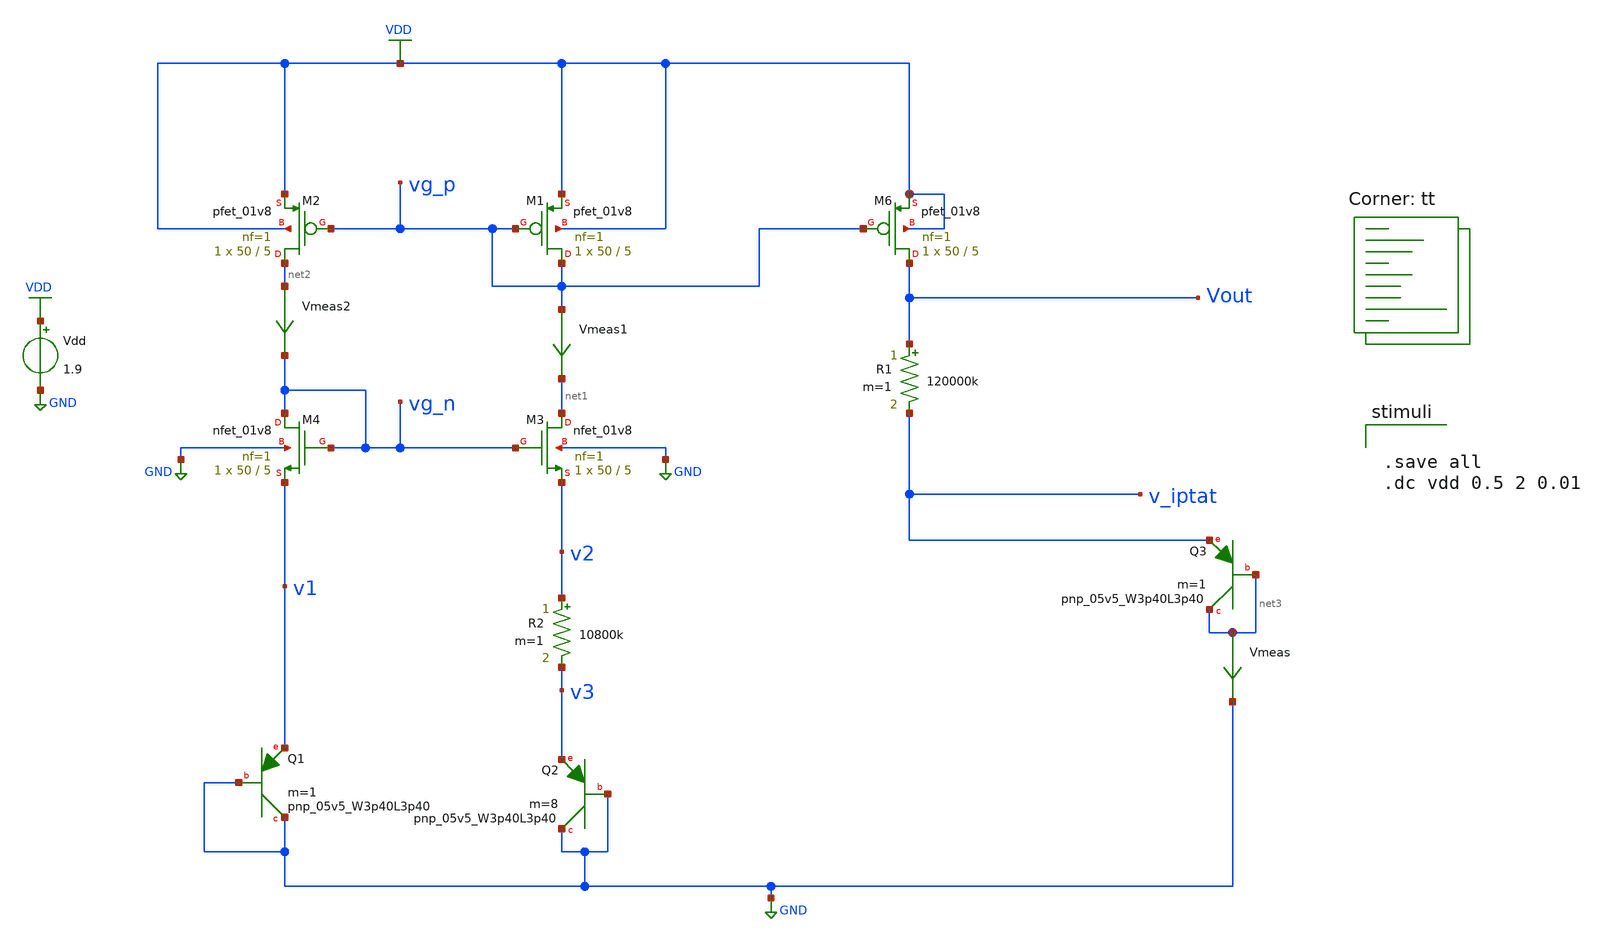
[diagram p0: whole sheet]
** sch_path: xschem/bandgap.sch
**.subckt bandgap
XM1 vg_p vg_p VDD VDD sky130_fd_pr__pfet_01v8 L=5 W=50 nf=1 ad='int((nf+1)/2) * W/nf * 0.29' as='int((nf+2)/2) * W/nf * 0.29'
+ pd='2*int((nf+1)/2) * (W/nf + 0.29)' ps='2*int((nf+2)/2) * (W/nf + 0.29)' nrd='0.29 / W' nrs='0.29 / W'
+ sa=0 sb=0 sd=0 mult=1 m=1
XM2 net2 vg_p VDD VDD sky130_fd_pr__pfet_01v8 L=5 W=50 nf=1 ad='int((nf+1)/2) * W/nf * 0.29' as='int((nf+2)/2) * W/nf * 0.29'
+ pd='2*int((nf+1)/2) * (W/nf + 0.29)' ps='2*int((nf+2)/2) * (W/nf + 0.29)' nrd='0.29 / W' nrs='0.29 / W'
+ sa=0 sb=0 sd=0 mult=1 m=1
XM3 net1 vg_n v2 GND sky130_fd_pr__nfet_01v8 L=5 W=50 nf=1 ad='int((nf+1)/2) * W/nf * 0.29' as='int((nf+2)/2) * W/nf * 0.29'
+ pd='2*int((nf+1)/2) * (W/nf + 0.29)' ps='2*int((nf+2)/2) * (W/nf + 0.29)' nrd='0.29 / W' nrs='0.29 / W'
+ sa=0 sb=0 sd=0 mult=1 m=1
XM4 vg_n vg_n v1 GND sky130_fd_pr__nfet_01v8 L=5 W=50 nf=1 ad='int((nf+1)/2) * W/nf * 0.29' as='int((nf+2)/2) * W/nf * 0.29'
+ pd='2*int((nf+1)/2) * (W/nf + 0.29)' ps='2*int((nf+2)/2) * (W/nf + 0.29)' nrd='0.29 / W' nrs='0.29 / W'
+ sa=0 sb=0 sd=0 mult=1 m=1
XQ1 GND GND v1 sky130_fd_pr__pnp_05v5_W3p40L3p40 m=1
Vdd VDD GND 1.9
XM6 Vout vg_p VDD VDD sky130_fd_pr__pfet_01v8 L=5 W=50 nf=1 ad='int((nf+1)/2) * W/nf * 0.29' as='int((nf+2)/2) * W/nf * 0.29'
+ pd='2*int((nf+1)/2) * (W/nf + 0.29)' ps='2*int((nf+2)/2) * (W/nf + 0.29)' nrd='0.29 / W' nrs='0.29 / W'
+ sa=0 sb=0 sd=0 mult=1 m=1
XQ3 net3 net3 v_iptat sky130_fd_pr__pnp_05v5_W3p40L3p40 m=1
R1 Vout v_iptat 120000k m=1
Vmeas net3 GND 0
.save i(vmeas)
Vmeas1 vg_p net1 0
.save i(vmeas1)
Vmeas2 net2 vg_n 0
.save i(vmeas2)
XQ2 GND GND v3 sky130_fd_pr__pnp_05v5_W3p40L3p40 m=8
R2 v2 v3 10800k m=1
**** begin user architecture code


.save all
.dc vdd 0.5 2 0.01


.lib $::SKYWATER_MODELS/sky130.lib.spice tt
**** end user architecture code
**.ends
.GLOBAL GND
.GLOBAL VDD
.end
